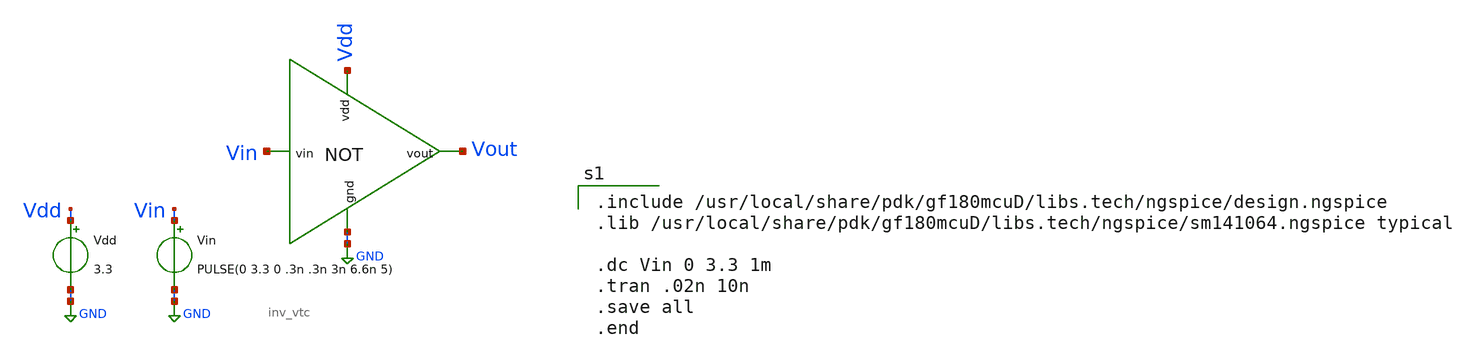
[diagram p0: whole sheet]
** sch_path: schem/inv_test.sch
**.subckt inv_test
Vin Vin GND PULSE(0 3.3 0 .3n .3n 3n 6.6n 5)
Vdd Vdd GND 3.3
x1 Vdd Vin Vout GND inv_vtc
**** begin user architecture code

.include /usr/local/share/pdk/gf180mcuD/libs.tech/ngspice/design.ngspice
.lib /usr/local/share/pdk/gf180mcuD/libs.tech/ngspice/sm141064.ngspice typical

.dc Vin 0 3.3 1m
.tran .02n 10n
.save all
.end


**** end user architecture code
**.ends

* expanding   symbol:  inv_vtc.sym # of pins=4
** sym_path: schem/inv_vtc.sym
** sch_path: schem/inv_vtc.sch
.subckt inv_vtc vdd vin vout gnd
*.ipin vin
*.ipin gnd
*.ipin vdd
*.opin vout
XM1 vout vin vdd vdd pfet_03v3 L=0.28u W=0.88u nf=1 ad='int((nf+1)/2) * W/nf * 0.18u' as='int((nf+2)/2) * W/nf * 0.18u'
+ pd='2*int((nf+1)/2) * (W/nf + 0.18u)' ps='2*int((nf+2)/2) * (W/nf + 0.18u)' nrd='0.18u / W' nrs='0.18u / W'
+ sa=0 sb=0 sd=0 m=1
XM2 vout vin gnd gnd nfet_03v3 L=0.28u W=0.22u nf=1 ad='int((nf+1)/2) * W/nf * 0.18u' as='int((nf+2)/2) * W/nf * 0.18u'
+ pd='2*int((nf+1)/2) * (W/nf + 0.18u)' ps='2*int((nf+2)/2) * (W/nf + 0.18u)' nrd='0.18u / W' nrs='0.18u / W'
+ sa=0 sb=0 sd=0 m=1
.ends

.GLOBAL GND
.end
